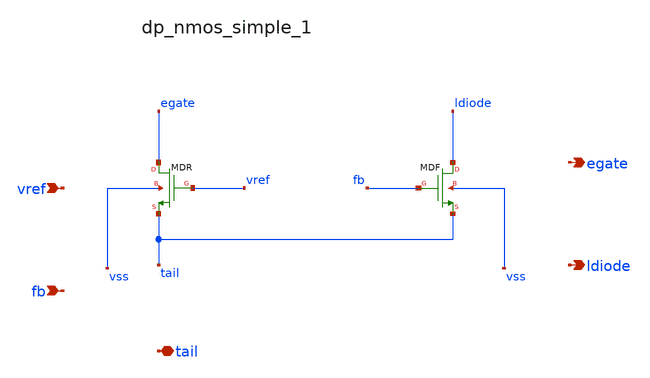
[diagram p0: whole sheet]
** sch_path: analog-db/raw/ldo_008_fer_mirror_ota/hier/blocks/dp_nmos_simple_1.sch
**.subckt dp_nmos_simple_1 vref fb tail egate ldiode
*.ipin vref
*.ipin fb
*.iopin tail
*.opin egate
*.opin ldiode
XMDF ldiode fb tail vss sg13_lv_nmos w=x_dut_xmdf_w l=x_dut_xmdf_l ng=1 m=x_dut_xmdf_m
XMDR egate vref tail vss sg13_lv_nmos w=x_dut_xmdr_w l=x_dut_xmdr_l ng=1 m=x_dut_xmdr_m
**.ends
.end
